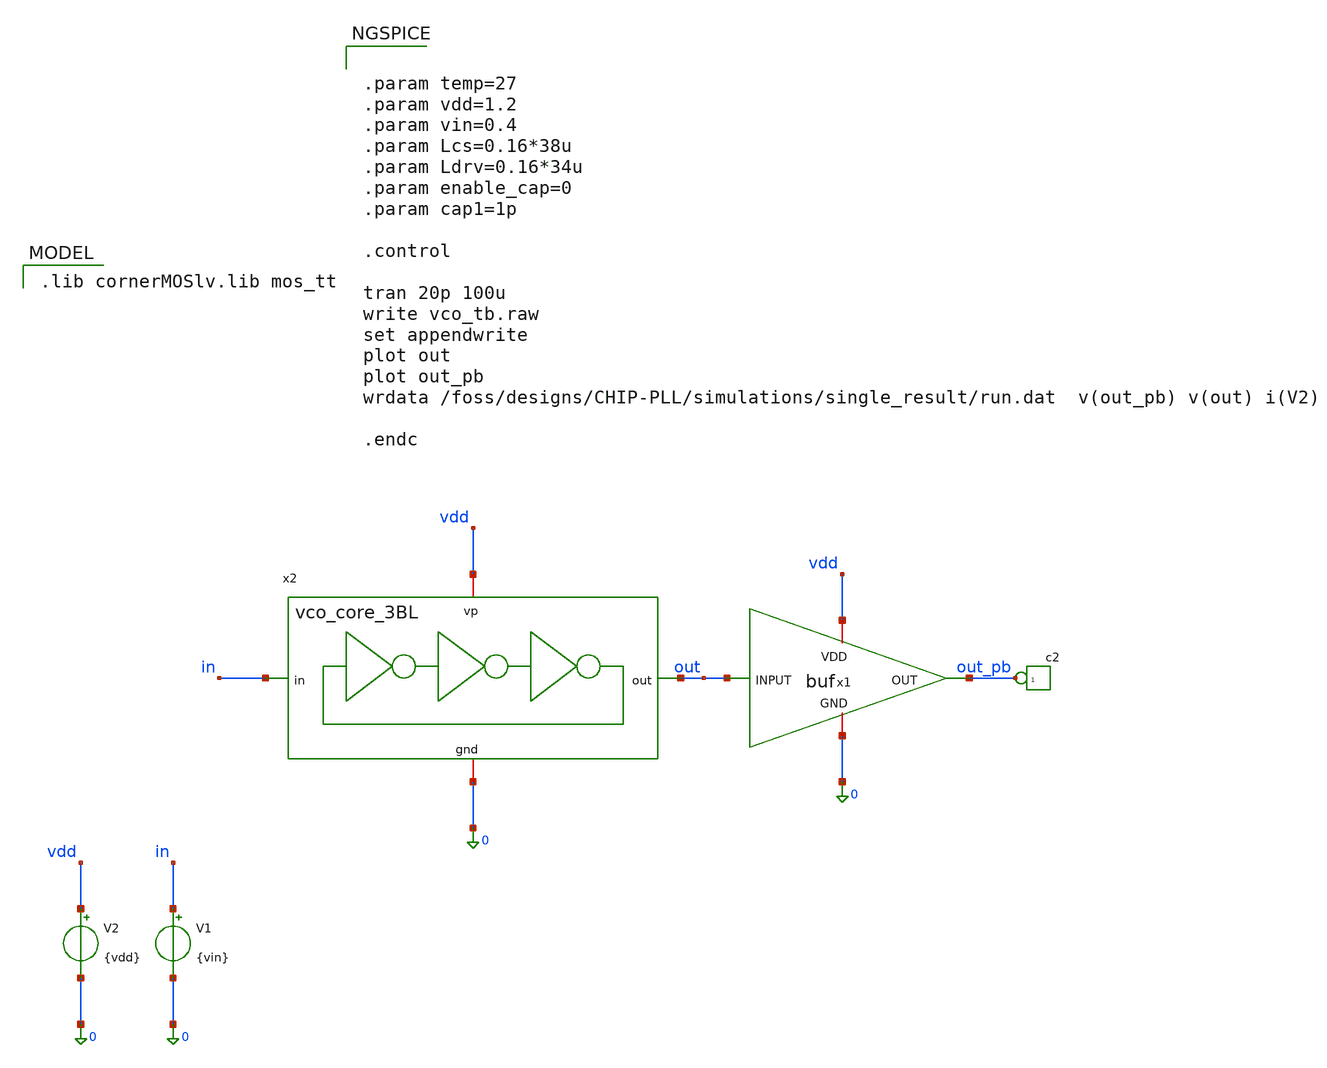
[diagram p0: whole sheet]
** sch_path: schematics/vco/vco_tb/vco_dcin_tb_3BL.sch
**.subckt vco_dcin_tb_3BL
V1 in 0 {vin}
V2 vdd 0 {vdd}
*connector(1,1) ?1 out_pb
x1 vdd out out_pb 0 buf
x2 vdd 0 out in vco_core_3BL
**** begin user architecture code


.param temp=27
.param vdd=1.2
.param vin=0.4
.param Lcs=0.16*38u
.param Ldrv=0.16*34u
.param enable_cap=0
.param cap1=1p

.control

tran 20p 100u
write vco_tb.raw
set appendwrite
plot out
plot out_pb
wrdata /foss/designs/CHIP-PLL/simulations/single_result/run.dat  v(out_pb) v(out) i(V2)

.endc


 .lib cornerMOSlv.lib mos_tt

**** end user architecture code
**.ends
.end
